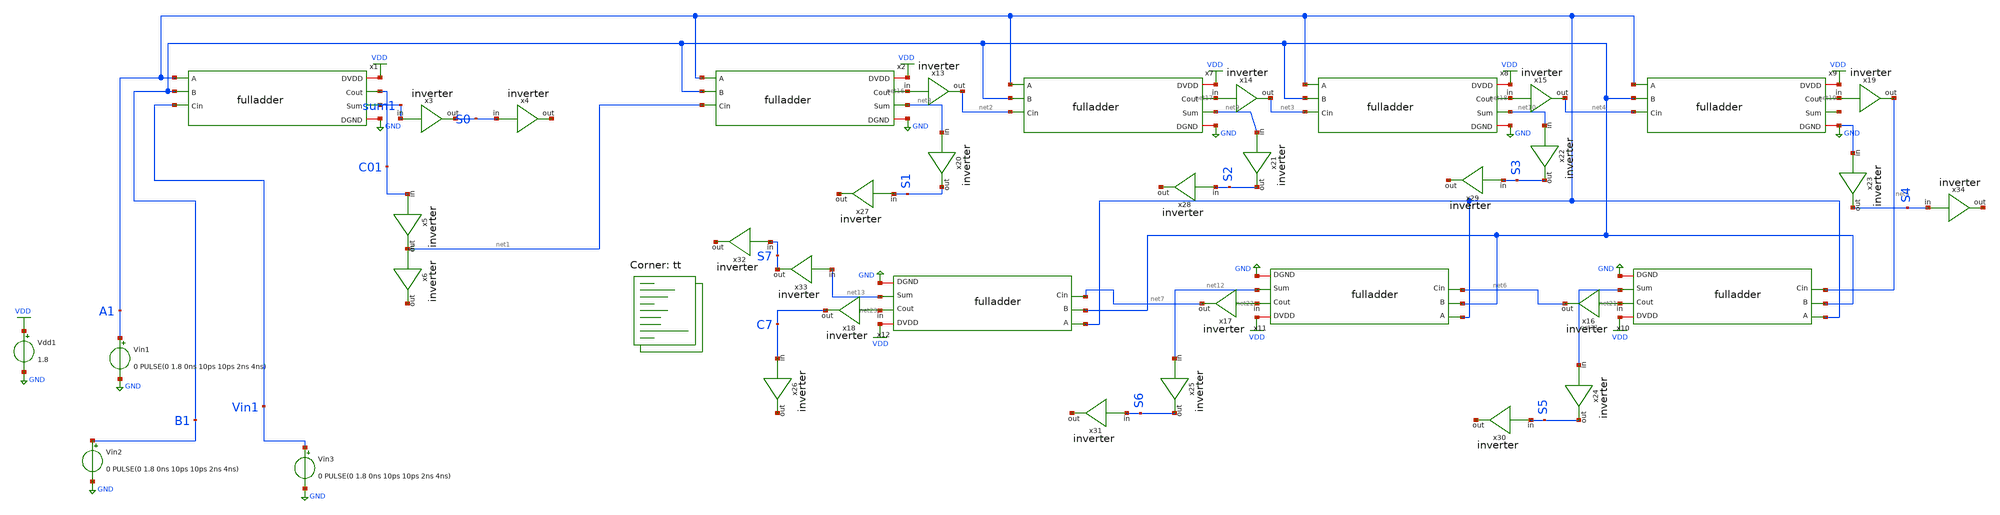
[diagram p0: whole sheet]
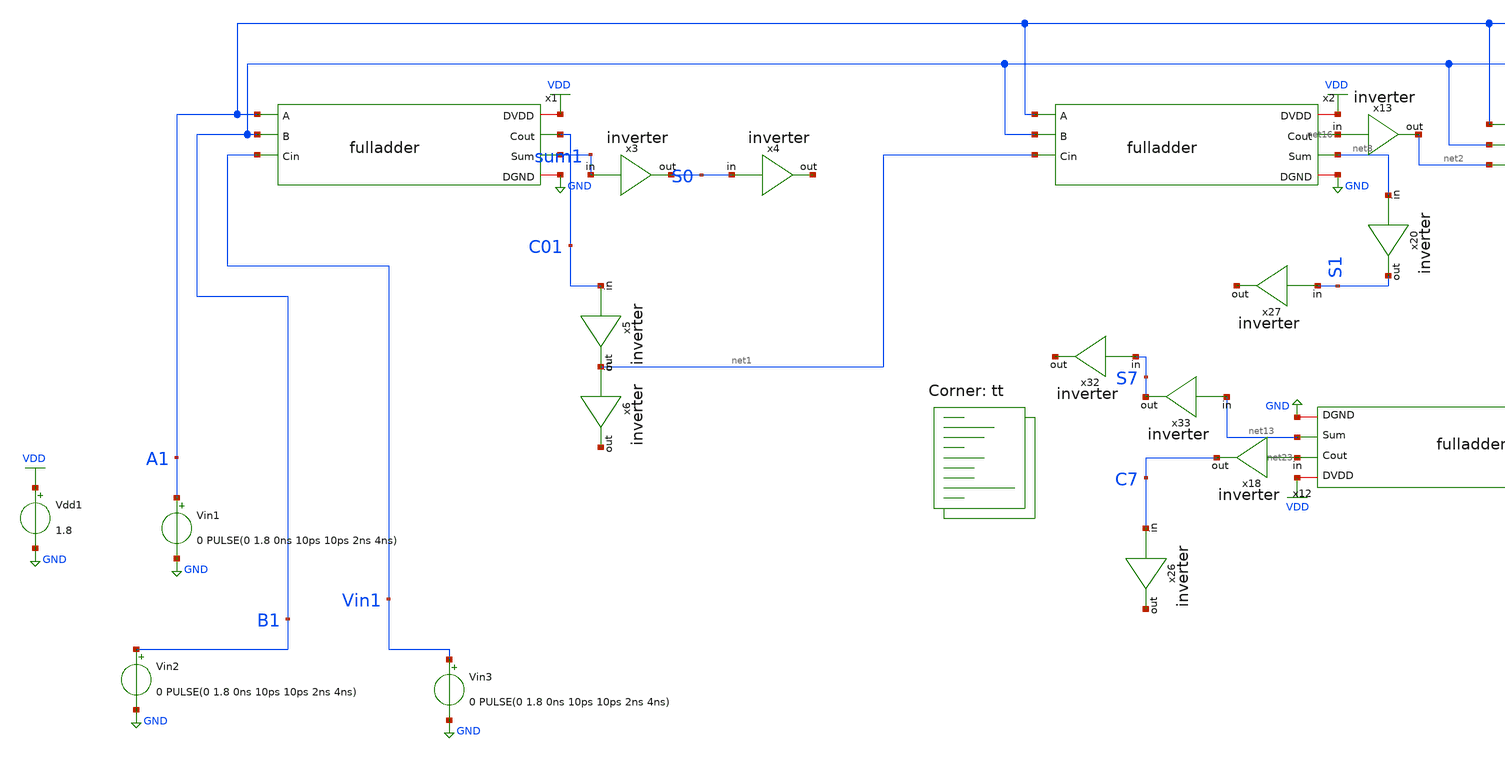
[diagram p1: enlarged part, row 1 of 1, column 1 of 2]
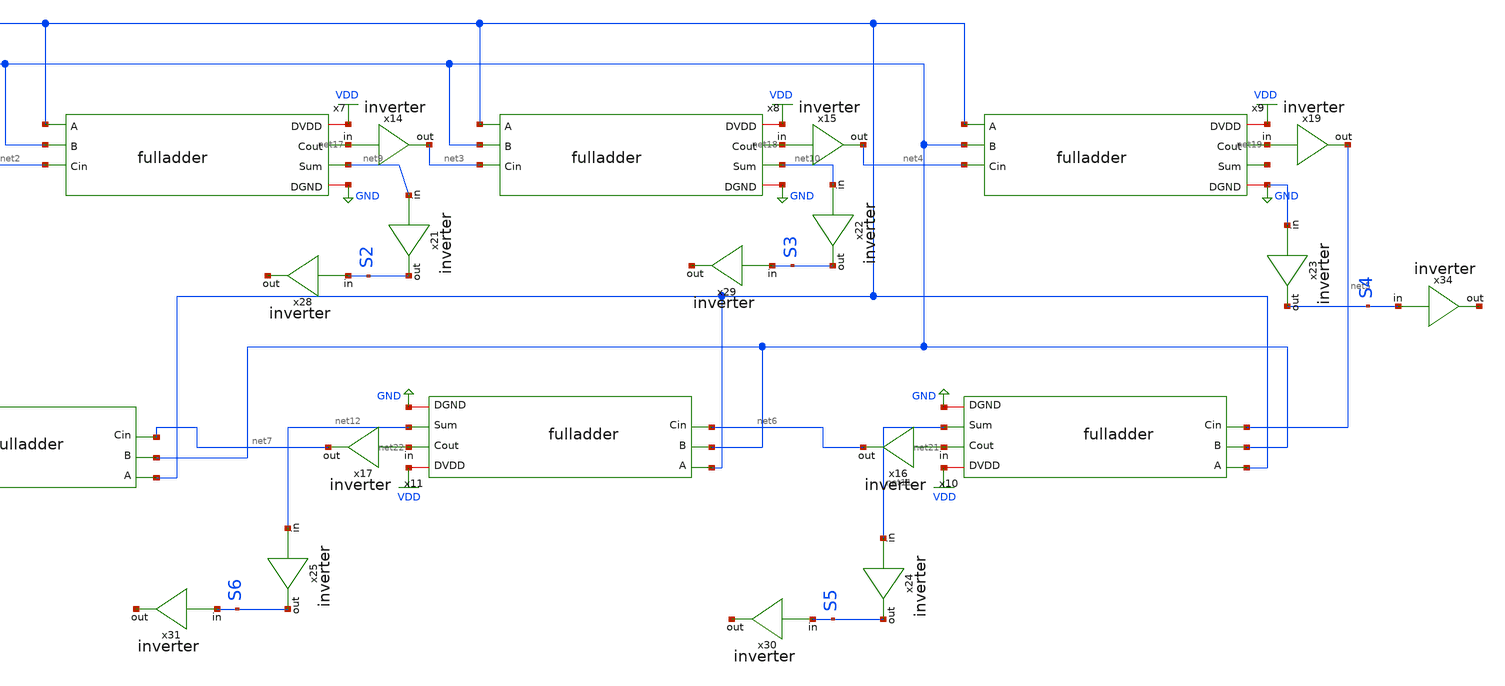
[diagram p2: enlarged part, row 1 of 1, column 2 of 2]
** sch_path: Tutorial_6/Part-B/ripple.sch
**.subckt ripple
x3 S0 sum1 inverter
Vdd1 VDD GND 1.8
x4 net14 S0 inverter
Vin2 B1 GND 0 PULSE(0 1.8 0ns 10ps 10ps 2ns 4ns)
x5 net1 C01 inverter
x6 net15 net1 inverter
x1 VDD A1 B1 Vin1 C01 sum1 GND fulladder
x2 VDD A1 B1 net1 net16 net8 GND fulladder
Vin1 A1 GND 0 PULSE(0 1.8 0ns 10ps 10ps 2ns 4ns)
Vin3 Vin1 GND 0 PULSE(0 1.8 0ns 10ps 10ps 2ns 4ns)
x7 VDD A1 B1 net2 net17 net9 GND fulladder
x8 VDD A1 B1 net3 net18 net10 GND fulladder
x9 VDD A1 B1 net4 net19 net20 GND fulladder
x10 VDD A1 B1 net5 net21 net11 GND fulladder
x11 VDD A1 B1 net6 net22 net12 GND fulladder
x12 VDD A1 B1 net7 net23 net13 GND fulladder
x13 net2 net16 inverter
x14 net3 net17 inverter
x15 net4 net18 inverter
x16 net6 net21 inverter
x17 net7 net22 inverter
x18 C7 net23 inverter
x19 net5 net19 inverter
x20 S1 net8 inverter
x21 S2 net9 inverter
x22 S3 net10 inverter
x23 S4 GND inverter
x24 S5 net11 inverter
x25 S6 net12 inverter
x26 net24 C7 inverter
x27 net25 S1 inverter
x28 net26 S2 inverter
x29 net27 S3 inverter
x30 net28 S5 inverter
x31 net29 S6 inverter
x32 net30 S7 inverter
x33 S7 net13 inverter
x34 net31 S4 inverter
**** begin user architecture code


*.include fulladder_extracted.spice
.control
tran 10ps 10ns
run
meas tran tplh TRIG V(Vin1) VAL=0.9 RISE=1 TARG V(C7) VAL=0.9 FALL=1
meas tran tpdhl TRIG V(Vin1) VAL=0.9 FALL=1 TARG V(C7) VAL=0.9 RISE=1
let tpd_Cout = ($&tplh + $&tpdhl)/2
meas tran tpd_Sumh TRIG V(Vin1) VAL=0.9 RISE=1 TARG V(S7) VAL=0.9 RISE=1
meas tran tpd_Suml TRIG V(Vin1) VAL=0.9 FALL=1 TARG V(S7) VAL=0.9 FALL=1
let tpd_Sum = ($&tpd_Sumh + $&tpd_Suml)/2

plot C01 C7 S0 S1 S2 S3 S4 S5 S6 S7
plot Vin1
plot A1
plot B1

echo Delay from Cin to C7: $&tpd_Cout
echo Delay from Cin to S7: $&tpd_Sum
.endc



.lib $::SKYWATER_MODELS/sky130.lib.spice tt
**** end user architecture code
**.ends
.GLOBAL GND
.GLOBAL VDD
.end
